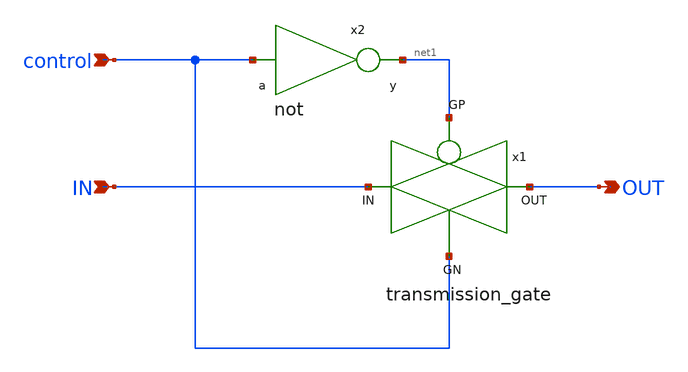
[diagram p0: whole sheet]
** sch_path: xschem/analog_switch.sch
* Copyright 2021 Stefan Frederik Schippers
* Licensed under the Apache License, Version 2.0 (the "License");
* you may not use this file except in compliance with the License.
* You may obtain a copy of the License at
* https://www.apache.org/licenses/LICENSE-2.0
* Unless required by applicable law or agreed to in writing, software
* distributed under the License is distributed on an "AS IS" BASIS,
* WITHOUT WARRANTIES OR CONDITIONS OF ANY KIND, either express or implied.
* See the License for the specific language governing permissions and
* limitations under the License.
**.subckt analog_switch IN control OUT
*.ipin IN
*.ipin control
*.opin OUT
x1 net1 OUT IN control transmission_gate
x2 control net1 not
**.ends

* expanding   symbol:  transmission_gate.sym # of pins=4
** sym_path: xschem/transmission_gate.sym
** sch_path: xschem/transmission_gate.sch
.subckt transmission_gate GP OUT IN GN
*.opin OUT
*.ipin IN
*.ipin GN
*.ipin GP
XM1 OUT GN IN GND sky130_fd_pr__nfet_01v8_lvt L=0.15 W=1 nf=1 ad='int((nf+1)/2) * W/nf * 0.29' as='int((nf+2)/2) * W/nf * 0.29'
+ pd='2*int((nf+1)/2) * (W/nf + 0.29)' ps='2*int((nf+2)/2) * (W/nf + 0.29)' nrd='0.29 / W' nrs='0.29 / W'
+ sa=0 sb=0 sd=0 mult=1 m=1
XM2 OUT GP IN VDD sky130_fd_pr__pfet_01v8_lvt L=0.35 W=1 nf=1 ad='int((nf+1)/2) * W/nf * 0.29' as='int((nf+2)/2) * W/nf * 0.29'
+ pd='2*int((nf+1)/2) * (W/nf + 0.29)' ps='2*int((nf+2)/2) * (W/nf + 0.29)' nrd='0.29 / W' nrs='0.29 / W'
+ sa=0 sb=0 sd=0 mult=1 m=1
.ends


* expanding   symbol:  not.sym # of pins=2
** sym_path: xschem/not.sym
** sch_path: xschem/not.sch
.subckt not a y
*.ipin a
*.opin y
XM1 y a GND GND sky130_fd_pr__nfet_01v8_lvt L=0.15 W=1 nf=1 ad='int((nf+1)/2) * W/nf * 0.29' as='int((nf+2)/2) * W/nf * 0.29'
+ pd='2*int((nf+1)/2) * (W/nf + 0.29)' ps='2*int((nf+2)/2) * (W/nf + 0.29)' nrd='0.29 / W' nrs='0.29 / W'
+ sa=0 sb=0 sd=0 mult=1 m=1
XM2 y a VDD VDD sky130_fd_pr__pfet_01v8_lvt L=0.35 W=1 nf=1 ad='int((nf+1)/2) * W/nf * 0.29' as='int((nf+2)/2) * W/nf * 0.29'
+ pd='2*int((nf+1)/2) * (W/nf + 0.29)' ps='2*int((nf+2)/2) * (W/nf + 0.29)' nrd='0.29 / W' nrs='0.29 / W'
+ sa=0 sb=0 sd=0 mult=1 m=1
.ends

.GLOBAL GND
.GLOBAL VDD
.end
